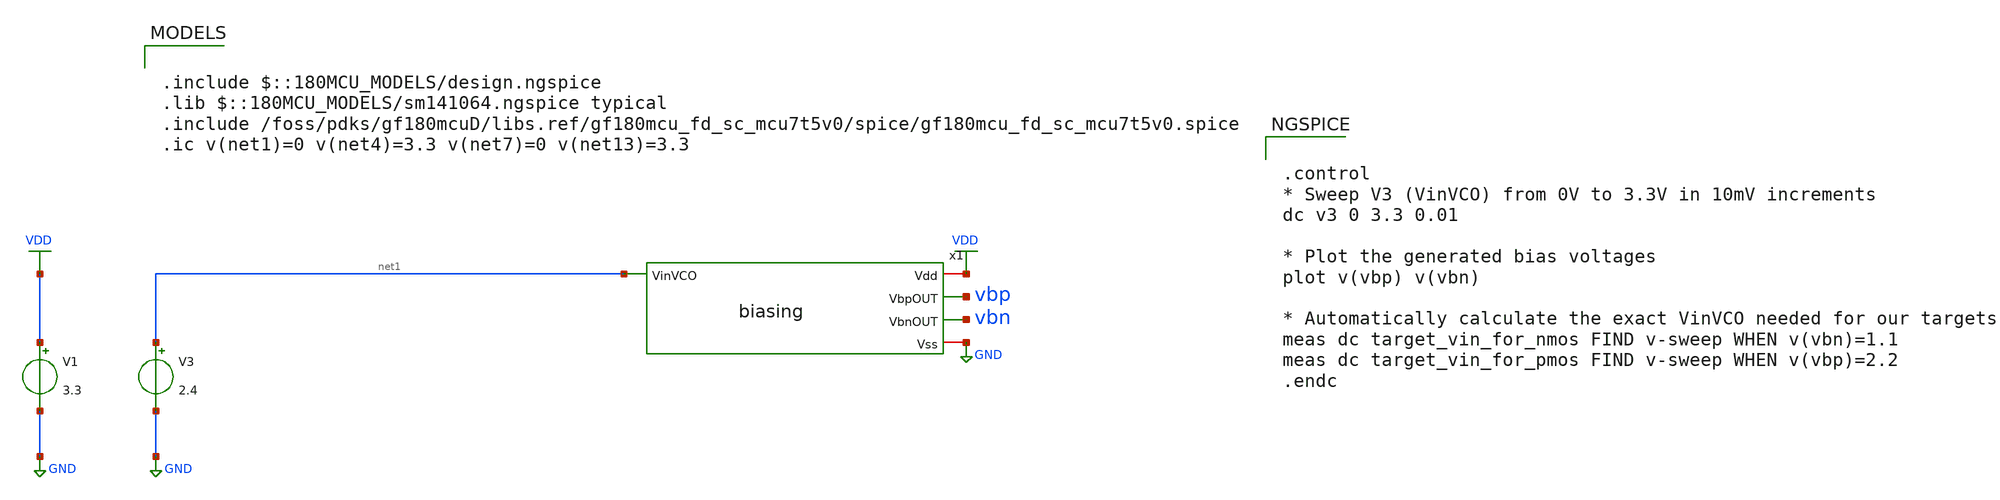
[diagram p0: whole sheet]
** sch_path: src/analog/biasing_tb.sch
**.subckt biasing_tb
x1 VDD vbp vbn net1 GND biasing
V1 VDD GND 3.3
V3 net1 GND 2.4
**** begin user architecture code

.include $::180MCU_MODELS/design.ngspice
.lib $::180MCU_MODELS/sm141064.ngspice typical
.include /foss/pdks/gf180mcuD/libs.ref/gf180mcu_fd_sc_mcu7t5v0/spice/gf180mcu_fd_sc_mcu7t5v0.spice
.ic v(net1)=0 v(net4)=3.3 v(net7)=0 v(net13)=3.3



.control
* Sweep V3 (VinVCO) from 0V to 3.3V in 10mV increments
dc v3 0 3.3 0.01

* Plot the generated bias voltages
plot v(vbp) v(vbn)

* Automatically calculate the exact VinVCO needed for our targets
meas dc target_vin_for_nmos FIND v-sweep WHEN v(vbn)=1.1
meas dc target_vin_for_pmos FIND v-sweep WHEN v(vbp)=2.2
.endc


**** end user architecture code
**.ends

* expanding   symbol:  biasing.sym # of pins=5
** sym_path: src/analog/biasing.sym
** sch_path: src/analog/biasing.sch
.subckt biasing Vdd VbpOUT VbnOUT VinVCO Vss
*.iopin Vdd
*.iopin Vss
*.ipin VinVCO
*.opin VbpOUT
*.opin VbnOUT
XM3 VbpOUT VbpOUT Vdd Vdd pfet_03v3 L=0.5u W=2u nf=1 ad='int((nf+1)/2) * W/nf * 0.18u' as='int((nf+2)/2) * W/nf * 0.18u'
+ pd='2*int((nf+1)/2) * (W/nf + 0.18u)' ps='2*int((nf+2)/2) * (W/nf + 0.18u)' nrd='0.18u / W' nrs='0.18u / W'
+ sa=0 sb=0 sd=0 m=1
XM4 VbpOUT VinVCO Vss Vss nfet_03v3 L=0.5u W=1u nf=1 ad='int((nf+1)/2) * W/nf * 0.18u' as='int((nf+2)/2) * W/nf * 0.18u'
+ pd='2*int((nf+1)/2) * (W/nf + 0.18u)' ps='2*int((nf+2)/2) * (W/nf + 0.18u)' nrd='0.18u / W' nrs='0.18u / W'
+ sa=0 sb=0 sd=0 m=1
XM1 VbnOUT VbpOUT Vdd Vdd pfet_03v3 L=0.5u W=2u nf=1 ad='int((nf+1)/2) * W/nf * 0.18u' as='int((nf+2)/2) * W/nf * 0.18u'
+ pd='2*int((nf+1)/2) * (W/nf + 0.18u)' ps='2*int((nf+2)/2) * (W/nf + 0.18u)' nrd='0.18u / W' nrs='0.18u / W'
+ sa=0 sb=0 sd=0 m=1
XM2 VbnOUT VbnOUT Vss Vss nfet_03v3 L=0.5u W=1u nf=1 ad='int((nf+1)/2) * W/nf * 0.18u' as='int((nf+2)/2) * W/nf * 0.18u'
+ pd='2*int((nf+1)/2) * (W/nf + 0.18u)' ps='2*int((nf+2)/2) * (W/nf + 0.18u)' nrd='0.18u / W' nrs='0.18u / W'
+ sa=0 sb=0 sd=0 m=1
.ends

.GLOBAL VDD
.GLOBAL GND
.end
